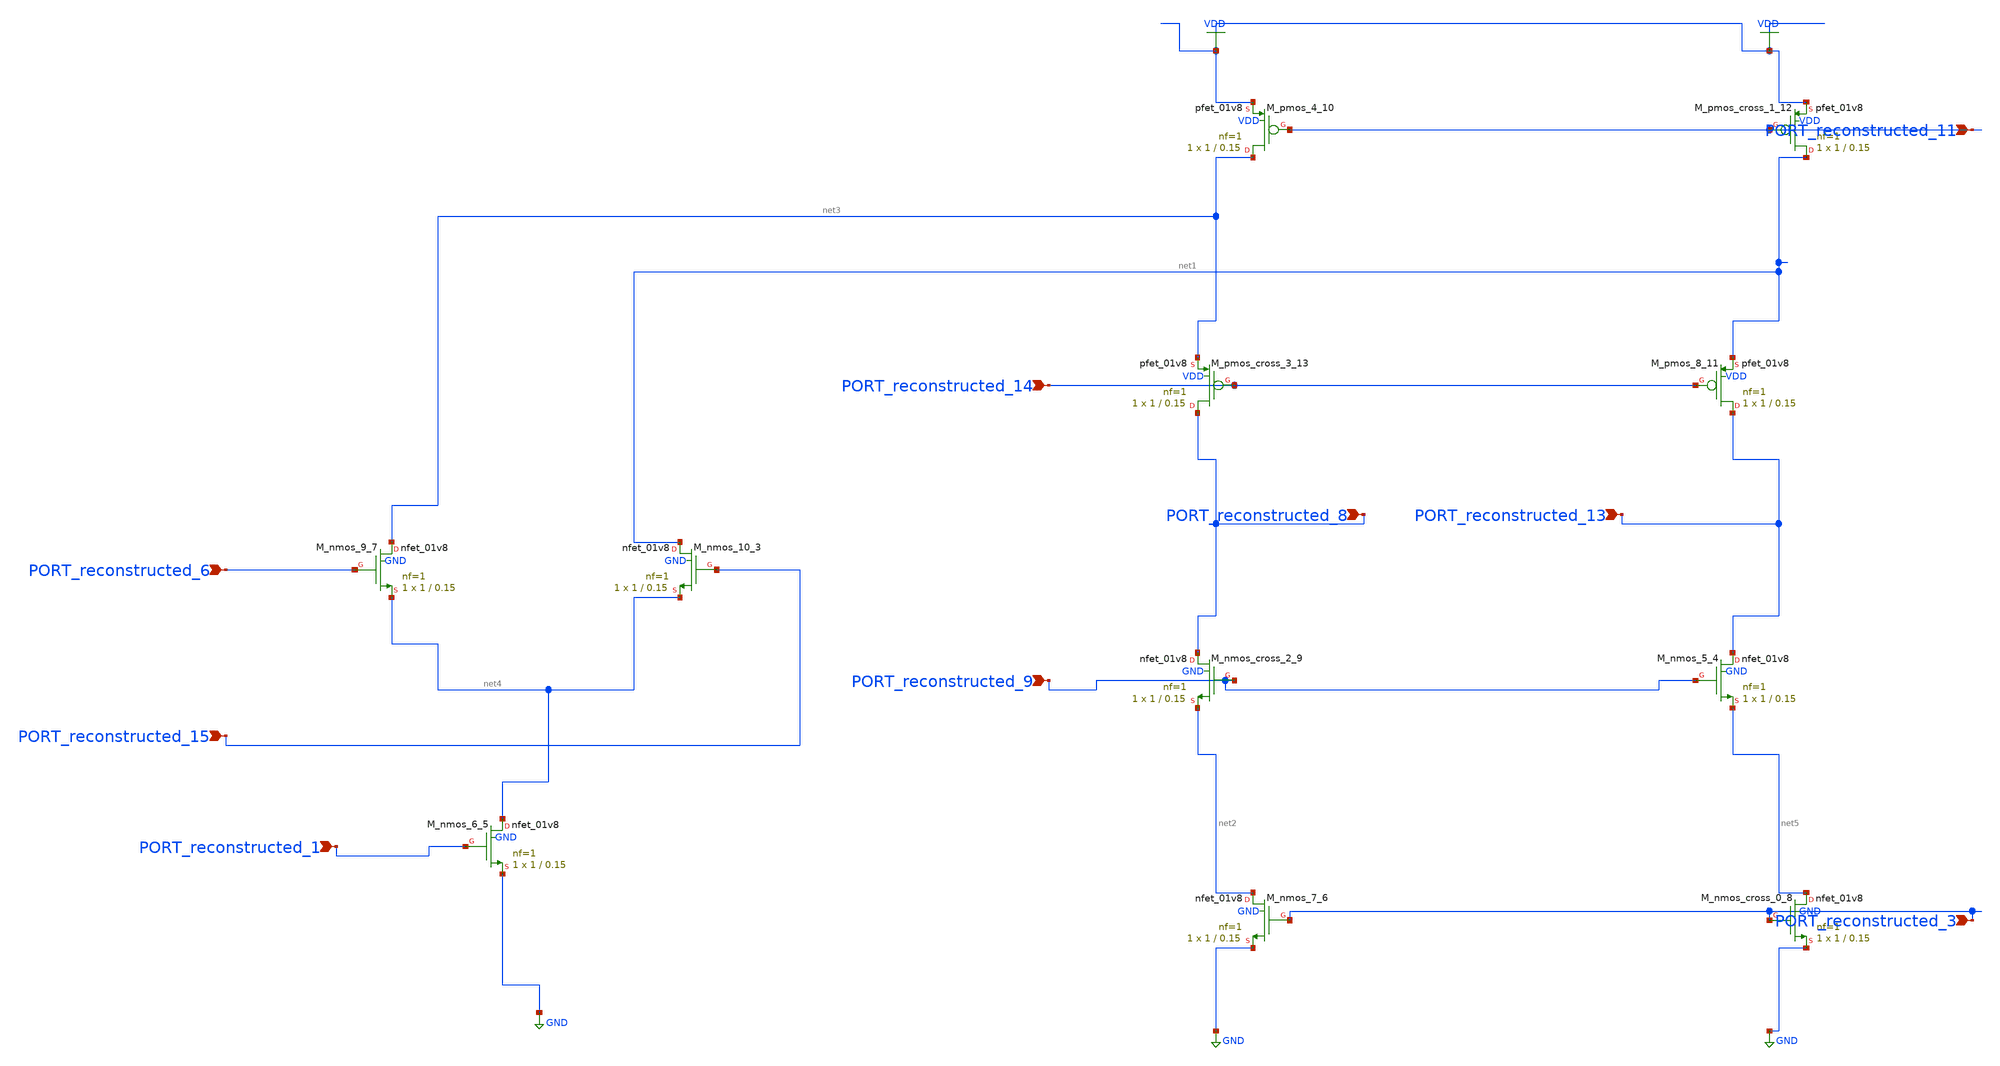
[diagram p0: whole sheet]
** sch_path: schematics/AMSNet/709.sch
**.subckt 709 PORT_reconstructed_8 PORT_reconstructed_13 PORT_reconstructed_6 PORT_reconstructed_15
*+ PORT_reconstructed_1 PORT_reconstructed_14 PORT_reconstructed_11 PORT_reconstructed_3 PORT_reconstructed_9
*.ipin PORT_reconstructed_8
*.ipin PORT_reconstructed_13
*.ipin PORT_reconstructed_6
*.ipin PORT_reconstructed_15
*.ipin PORT_reconstructed_1
*.ipin PORT_reconstructed_14
*.ipin PORT_reconstructed_11
*.ipin PORT_reconstructed_3
*.ipin PORT_reconstructed_9
XM_nmos_10_3 net1 PORT_reconstructed_15 net4 GND sky130_fd_pr__nfet_01v8 L=0.15 W=1 nf=1 ad='int((1 + 1)/2) * 1 / 1 * 0.29'
+ as='int((1 + 2)/2) * 1 / 1 * 0.29' pd='2*int((1 + 1)/2) * (1 / 1 + 0.29)' ps='2*int((1 + 2)/2) * (1 / 1 + 0.29)'
+ nrd='0.29 / 1 ' nrs='0.29 / 1 ' sa=0 sb=0 sd=0 mult=1 m=1
XM_nmos_5_4 PORT_reconstructed_13 PORT_reconstructed_9 net5 GND sky130_fd_pr__nfet_01v8 L=0.15 W=1 nf=1
+ ad='int((1 + 1)/2) * 1 / 1 * 0.29' as='int((1 + 2)/2) * 1 / 1 * 0.29' pd='2*int((1 + 1)/2) * (1 / 1 + 0.29)'
+ ps='2*int((1 + 2)/2) * (1 / 1 + 0.29)' nrd='0.29 / 1 ' nrs='0.29 / 1 ' sa=0 sb=0 sd=0 mult=1 m=1
XM_nmos_6_5 net4 PORT_reconstructed_1 GND GND sky130_fd_pr__nfet_01v8 L=0.15 W=1 nf=1 ad='int((1 + 1)/2) * 1 / 1 * 0.29'
+ as='int((1 + 2)/2) * 1 / 1 * 0.29' pd='2*int((1 + 1)/2) * (1 / 1 + 0.29)' ps='2*int((1 + 2)/2) * (1 / 1 + 0.29)'
+ nrd='0.29 / 1 ' nrs='0.29 / 1 ' sa=0 sb=0 sd=0 mult=1 m=1
XM_nmos_7_6 net2 PORT_reconstructed_3 GND GND sky130_fd_pr__nfet_01v8 L=0.15 W=1 nf=1 ad='int((1 + 1)/2) * 1 / 1 * 0.29'
+ as='int((1 + 2)/2) * 1 / 1 * 0.29' pd='2*int((1 + 1)/2) * (1 / 1 + 0.29)' ps='2*int((1 + 2)/2) * (1 / 1 + 0.29)'
+ nrd='0.29 / 1 ' nrs='0.29 / 1 ' sa=0 sb=0 sd=0 mult=1 m=1
XM_nmos_9_7 net3 PORT_reconstructed_6 net4 GND sky130_fd_pr__nfet_01v8 L=0.15 W=1 nf=1 ad='int((1 + 1)/2) * 1 / 1 * 0.29'
+ as='int((1 + 2)/2) * 1 / 1 * 0.29' pd='2*int((1 + 1)/2) * (1 / 1 + 0.29)' ps='2*int((1 + 2)/2) * (1 / 1 + 0.29)'
+ nrd='0.29 / 1 ' nrs='0.29 / 1 ' sa=0 sb=0 sd=0 mult=1 m=1
XM_nmos_cross_0_8 net5 PORT_reconstructed_3 GND GND sky130_fd_pr__nfet_01v8 L=0.15 W=1 nf=1 ad='int((1 + 1)/2) * 1 / 1 * 0.29'
+ as='int((1 + 2)/2) * 1 / 1 * 0.29' pd='2*int((1 + 1)/2) * (1 / 1 + 0.29)' ps='2*int((1 + 2)/2) * (1 / 1 + 0.29)'
+ nrd='0.29 / 1 ' nrs='0.29 / 1 ' sa=0 sb=0 sd=0 mult=1 m=1
XM_nmos_cross_2_9 PORT_reconstructed_8 PORT_reconstructed_9 net2 GND sky130_fd_pr__nfet_01v8 L=0.15 W=1
+ nf=1 ad='int((1 + 1)/2) * 1 / 1 * 0.29' as='int((1 + 2)/2) * 1 / 1 * 0.29' pd='2*int((1 + 1)/2) * (1 / 1 + 0.29)'
+ ps='2*int((1 + 2)/2) * (1 / 1 + 0.29)' nrd='0.29 / 1 ' nrs='0.29 / 1 ' sa=0 sb=0 sd=0 mult=1 m=1
XM_pmos_4_10 net3 PORT_reconstructed_11 VDD VDD sky130_fd_pr__pfet_01v8 L=0.15 W=1 nf=1 ad='int((1 + 1)/2) * 1 / 1 * 0.29'
+ as='int((1 + 2)/2) * 1 / 1 * 0.29' pd='2*int((1 + 1)/2) * (1 / 1 + 0.29)' ps='2*int((1 + 2)/2) * (1 / 1 + 0.29)'
+ nrd='0.29 / 1 ' nrs='0.29 / 1 ' sa=0 sb=0 sd=0 mult=1 m=1
XM_pmos_8_11 PORT_reconstructed_13 PORT_reconstructed_14 net1 VDD sky130_fd_pr__pfet_01v8 L=0.15 W=1
+ nf=1 ad='int((1 + 1)/2) * 1 / 1 * 0.29' as='int((1 + 2)/2) * 1 / 1 * 0.29' pd='2*int((1 + 1)/2) * (1 / 1 + 0.29)'
+ ps='2*int((1 + 2)/2) * (1 / 1 + 0.29)' nrd='0.29 / 1 ' nrs='0.29 / 1 ' sa=0 sb=0 sd=0 mult=1 m=1
XM_pmos_cross_1_12 net1 PORT_reconstructed_11 VDD VDD sky130_fd_pr__pfet_01v8 L=0.15 W=1 nf=1 ad='int((1 + 1)/2) * 1 / 1 * 0.29'
+ as='int((1 + 2)/2) * 1 / 1 * 0.29' pd='2*int((1 + 1)/2) * (1 / 1 + 0.29)' ps='2*int((1 + 2)/2) * (1 / 1 + 0.29)'
+ nrd='0.29 / 1 ' nrs='0.29 / 1 ' sa=0 sb=0 sd=0 mult=1 m=1
XM_pmos_cross_3_13 PORT_reconstructed_8 PORT_reconstructed_14 net3 VDD sky130_fd_pr__pfet_01v8 L=0.15
+ W=1 nf=1 ad='int((1 + 1)/2) * 1 / 1 * 0.29' as='int((1 + 2)/2) * 1 / 1 * 0.29' pd='2*int((1 + 1)/2) * (1 / 1 + 0.29)'
+ ps='2*int((1 + 2)/2) * (1 / 1 + 0.29)' nrd='0.29 / 1 ' nrs='0.29 / 1 ' sa=0 sb=0 sd=0 mult=1 m=1
**.ends
.GLOBAL GND
.GLOBAL VDD
.end
